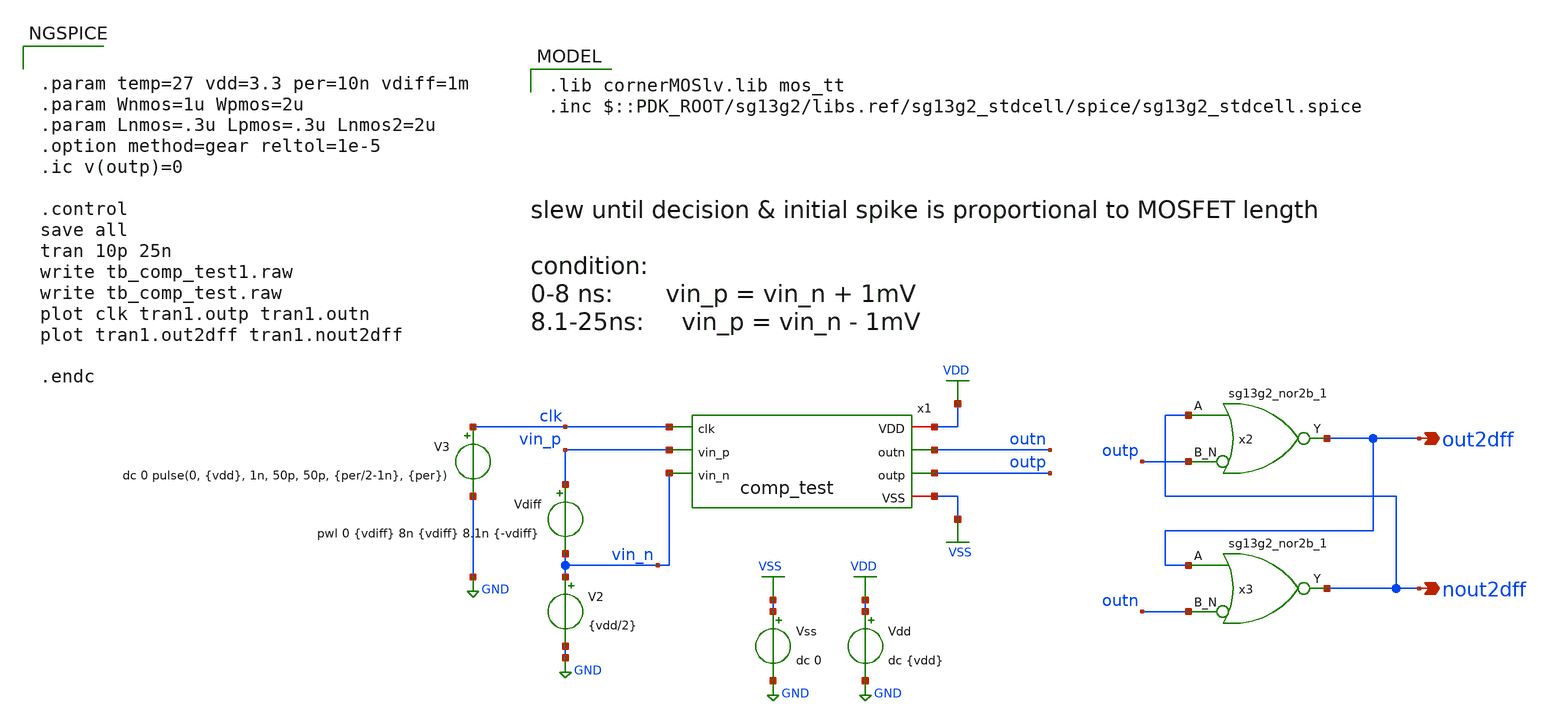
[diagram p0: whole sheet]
** sch_path: design/design_comp/tb_comp_test.sch
**.subckt tb_comp_test out2dff nout2dff
*.opin out2dff
*.opin nout2dff
x1 VDD clk outn outp vin_p vin_n VSS comp_test
V2 vin_n GND {vdd/2}
V3 clk GND dc 0 pulse(0, {vdd}, 1n, 50p, 50p, {per/2-1n}, {per})
Vdiff vin_p vin_n pwl 0 {vdiff} 8n {vdiff} 8.1n {-vdiff}
Vdd VDD GND dc {vdd}
Vss VSS GND dc 0
x2 out2dff nout2dff outp VDD VSS sg13g2_nor2b_1
x3 nout2dff out2dff outn VDD VSS sg13g2_nor2b_1
**** begin user architecture code
 .lib cornerMOSlv.lib mos_tt
.inc $::PDK_ROOT/sg13g2/libs.ref/sg13g2_stdcell/spice/sg13g2_stdcell.spice


.param temp=27 vdd=3.3 per=10n vdiff=1m
.param Wnmos=1u Wpmos=2u
.param Lnmos=.3u Lpmos=.3u Lnmos2=2u
.option method=gear reltol=1e-5
.ic v(outp)=0

.control
save all
tran 10p 25n
write tb_comp_test1.raw
write tb_comp_test.raw
plot clk tran1.outp tran1.outn
plot tran1.out2dff tran1.nout2dff

.endc

**** end user architecture code
**.ends

* expanding   symbol:  comp_test.sym # of pins=7
** sym_path: design/design_comp/comp_test.sym
** sch_path: design/design_comp/comp_test.sch
.subckt comp_test VDD clk outn outp vin_p vin_n VSS
*.ipin clk
*.iopin VSS
*.iopin VDD
*.ipin vin_n
*.ipin vin_p
*.opin outn
*.opin outp
XM5p outn clk VDD VDD sg13_lv_pmos w=Wpmos l=Lpmos ng=1 m=1 mm_ok=1
XM4n outp outn VDD VDD sg13_lv_pmos w=Wpmos l=Lpmos ng=1 m=1 mm_ok=1
XM4p outn outp VDD VDD sg13_lv_pmos w=Wpmos l=Lpmos ng=1 m=1 mm_ok=1
XM5n outp clk VDD VDD sg13_lv_pmos w=Wpmos l=Lpmos ng=1 m=1 mm_ok=1
XM3p d2p outp outn VSS sg13_lv_nmos w=Wnmos l=Lnmos ng=1 m=1 mm_ok=1
XM3n d2m outn outp VSS sg13_lv_nmos w=Wnmos l=Lnmos ng=1 m=1 mm_ok=1
XM2n d1m clk d2m VSS sg13_lv_nmos w=Wnmos l=Lnmos ng=1 m=1 mm_ok=1
XM2p d1p clk d2p VSS sg13_lv_nmos w=Wnmos l=Lnmos ng=1 m=1 mm_ok=1
XM1n VSS vin_n d1m VSS sg13_lv_nmos w=Wnmos l=Lnmos2 ng=1 m=1 mm_ok=1
XM1p VSS vin_p d1p VSS sg13_lv_nmos w=Wnmos l=Lnmos2 ng=1 m=1 mm_ok=1
.ends


* expanding   symbol:  sg13g2_stdcells/sg13g2_nor2b_1.sym # of pins=3
** sym_path: sg13g2_stdcells/sg13g2_nor2b_1.sym
** sch_path: sg13g2_stdcells/sg13g2_nor2b_1.sch
.subckt sg13g2_nor2b_1 Y A B_N VDD VSS
*.opin Y
*.ipin B_N
*.ipin A
*.iopin VDD
*.iopin VSS
XM1 B B_N VSS VSS sg13_lv_nmos w=550.00n l=130.00n ng=1 m=1 mm_ok=1
XM2 Y A VSS VSS sg13_lv_nmos w=740.00n l=130.00n ng=1 m=1 mm_ok=1
XM3 Y B VSS VSS sg13_lv_nmos w=740.00n l=130.00n ng=1 m=1 mm_ok=1
XM4 B B_N VDD VDD sg13_lv_pmos w=840.00n l=130.00n ng=1 m=1 mm_ok=1
XM5 net1 B VDD VDD sg13_lv_pmos w=1.12u l=130.00n ng=1 m=1 mm_ok=1
XM6 Y A net1 VDD sg13_lv_pmos w=1.12u l=130.00n ng=1 m=1 mm_ok=1
.ends

.GLOBAL GND
.GLOBAL VDD
.GLOBAL VSS
.end
